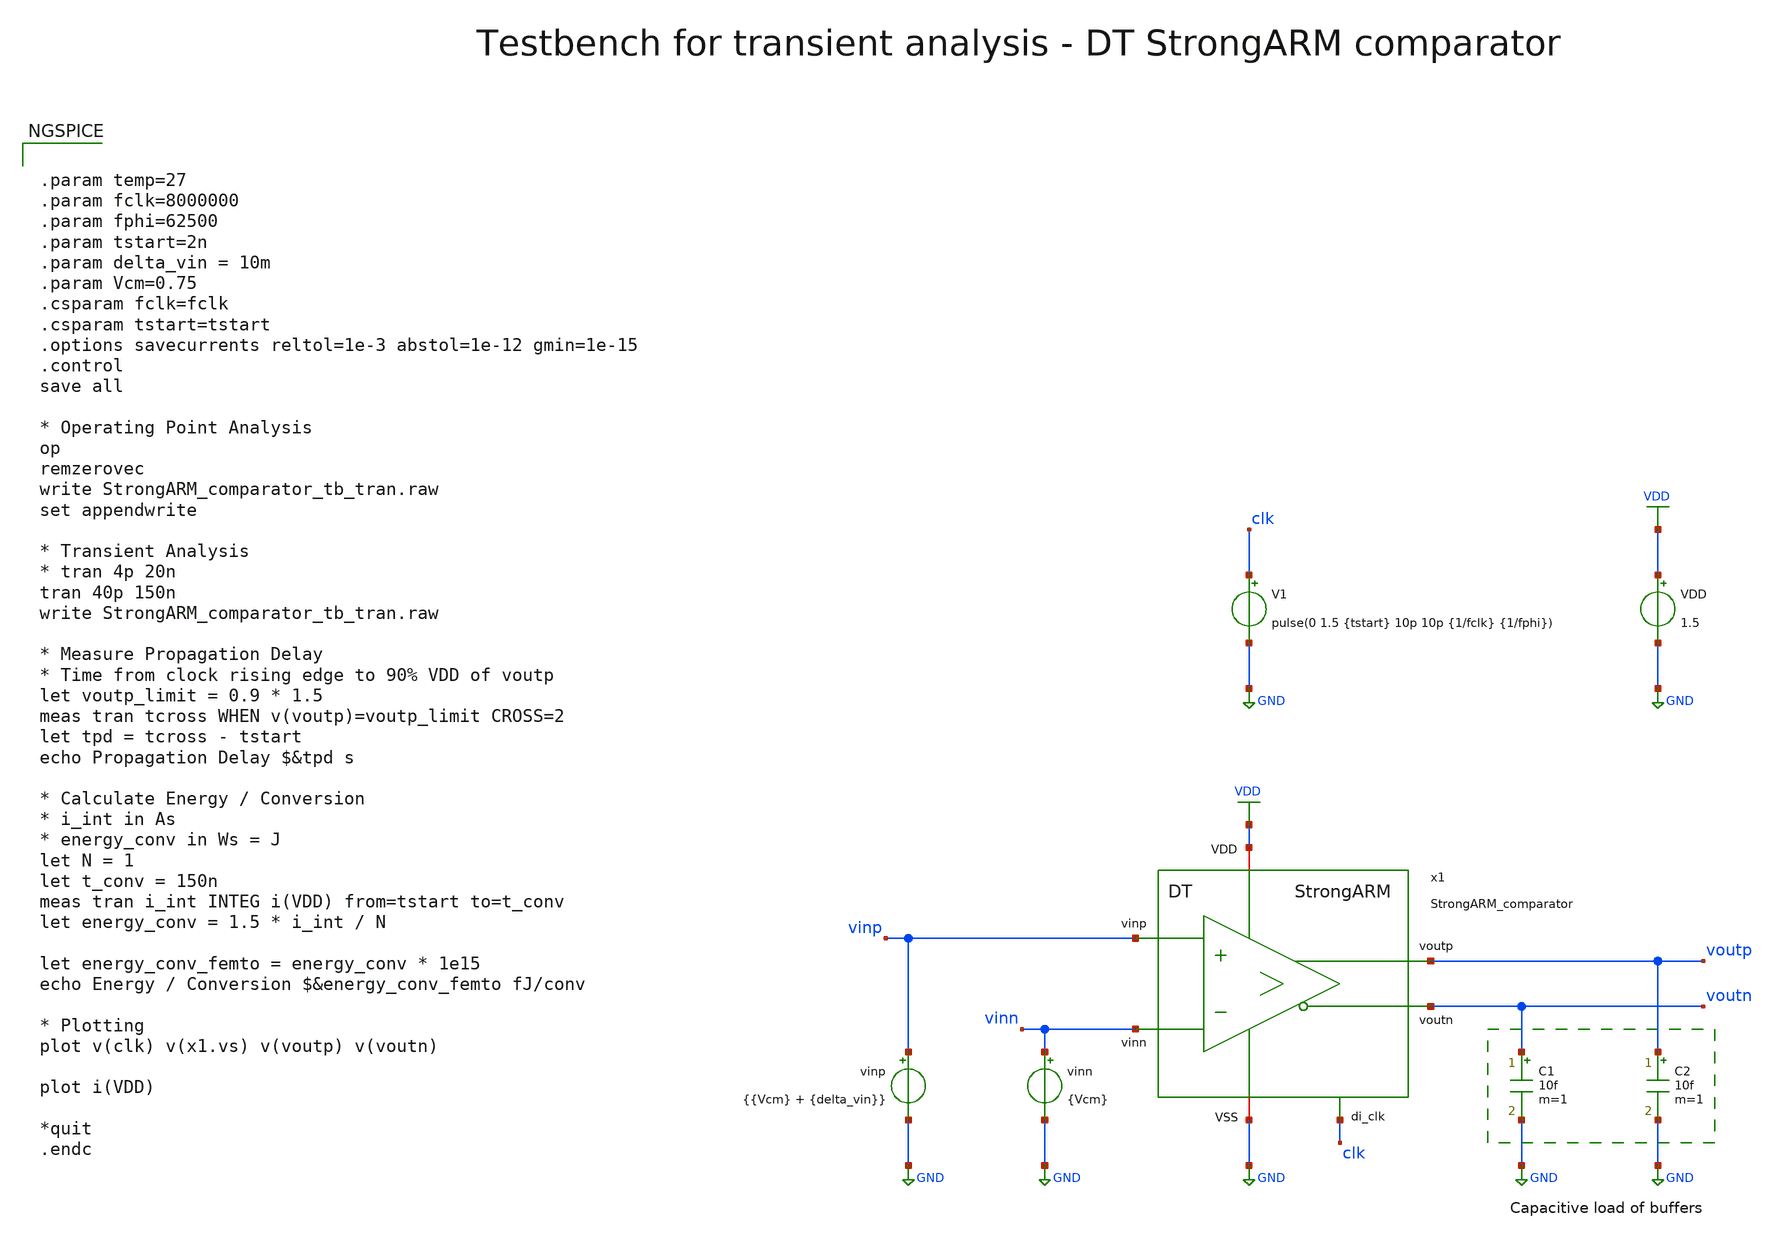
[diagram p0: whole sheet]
** sch_path: SG13G2_ATBS-ADC-main/xschem/comparator/discrete_time/StrongARM/testbenches/StrongARM_comparator_tb_tran.sch
**.subckt StrongARM_comparator_tb_tran
VDD VDD GND 1.5
V1 clk GND pulse(0 1.5 {tstart} 10p 10p {1/fclk} {1/fphi})
vinn vinn GND {Vcm}
vinp vinp GND {{Vcm} + {delta_vin}}
C1 voutn GND 10f m=1
C2 voutp GND 10f m=1
x1 clk VDD voutp vinp GND voutn vinn StrongARM_comparator
**** begin user architecture code

.lib cornerMOSlv.lib mos_tt
.lib cornerMOShv.lib mos_tt
.lib cornerRES.lib res_typ



.param temp=27
.param fclk=8000000
.param fphi=62500
.param tstart=2n
.param delta_vin = 10m
.param Vcm=0.75
.csparam fclk=fclk
.csparam tstart=tstart
.options savecurrents reltol=1e-3 abstol=1e-12 gmin=1e-15
.control
save all

* Operating Point Analysis
op
remzerovec
write StrongARM_comparator_tb_tran.raw
set appendwrite

* Transient Analysis
* tran 4p 20n
tran 40p 150n
write StrongARM_comparator_tb_tran.raw

* Measure Propagation Delay
* Time from clock rising edge to 90% VDD of voutp
let voutp_limit = 0.9 * 1.5
meas tran tcross WHEN v(voutp)=voutp_limit CROSS=2
let tpd = tcross - tstart
echo Propagation Delay $&tpd s

* Calculate Energy / Conversion
* i_int in As
* energy_conv in Ws = J
let N = 1
let t_conv = 150n
meas tran i_int INTEG i(VDD) from=tstart to=t_conv
let energy_conv = 1.5 * i_int / N

let energy_conv_femto = energy_conv * 1e15
echo Energy / Conversion $&energy_conv_femto fJ/conv

* Plotting
plot v(clk) v(x1.vs) v(voutp) v(voutn)

plot i(VDD)

*quit
.endc

**** end user architecture code
**.ends

* expanding   symbol:  comparator/discrete_time/StrongARM/StrongARM_comparator.sym # of pins=7
** sym_path: SG13G2_ATBS-ADC-main/xschem/comparator/discrete_time/StrongARM/StrongARM_comparator.sym
** sch_path: SG13G2_ATBS-ADC-main/xschem/comparator/discrete_time/StrongARM/StrongARM_comparator.sch
.subckt StrongARM_comparator di_clk VDD voutp vinp VSS voutn vinn
*.iopin VDD
*.opin voutp
*.iopin VSS
*.opin voutn
*.ipin vinp
*.ipin vinn
*.ipin di_clk
XM1 net1 vinp vs VSS sg13_lv_nmos w=1.0u l=0.13u ng=1 m=1 mm_ok=1
XM2 net2 vinn vs VSS sg13_lv_nmos w=1.0u l=0.13u ng=1 m=1 mm_ok=1
XM3 voutn voutp net1 VSS sg13_lv_nmos w=1.0u l=0.13u ng=1 m=1 mm_ok=1
XM4 voutp voutn net2 VSS sg13_lv_nmos w=1.0u l=0.13u ng=1 m=1 mm_ok=1
XM5 voutn voutp VDD VDD sg13_lv_pmos w=1.0u l=0.13u ng=1 m=1 mm_ok=1
XM6 voutp voutn VDD VDD sg13_lv_pmos w=1.0u l=0.13u ng=1 m=1 mm_ok=1
XM7 vs di_clk VSS VSS sg13_lv_nmos w=1.0u l=0.13u ng=1 m=1 mm_ok=1
XM8 voutn di_clk VDD VDD sg13_lv_pmos w=1.0u l=0.13u ng=1 m=1 mm_ok=1
XM9 net1 di_clk VDD VDD sg13_lv_pmos w=1.0u l=0.13u ng=1 m=1 mm_ok=1
XM10 voutp di_clk VDD VDD sg13_lv_pmos w=1.0u l=0.13u ng=1 m=1 mm_ok=1
XM11 net2 di_clk VDD VDD sg13_lv_pmos w=1.0u l=0.13u ng=1 m=1 mm_ok=1
CPn voutn VSS 300f m=1
CPp voutp VSS 300f m=1
.ends

.GLOBAL GND
.GLOBAL VDD
.end
